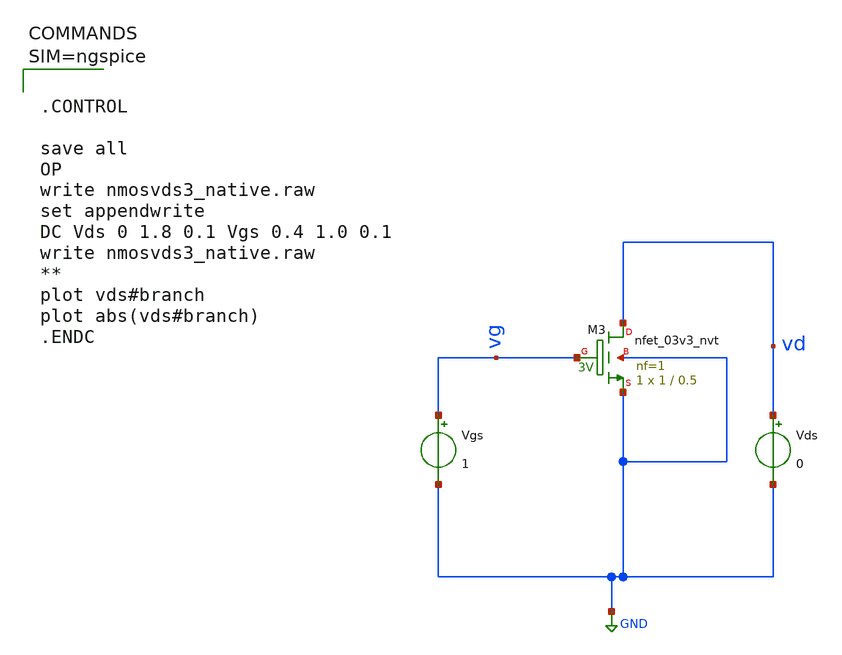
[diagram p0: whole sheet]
** sch_path: work/xschem/nmosvds3_native.sch
**.subckt nmosvds3_native
Vgs vg GND 1
Vds vd GND 0
XM3 vd vg GND GND sky130_fd_pr__nfet_03v3_nvt L=0.5 W=1 nf=1 ad='int((1 + 1)/2) * 1 / 1 * 0.29' as='int((1 + 2)/2) * 1 / 1 * 0.29'
+ pd='2*int((1 + 1)/2) * (1 / 1 + 0.29)' ps='2*int((1 + 2)/2) * (1 / 1 + 0.29)' nrd='0.29 / 1 ' nrs='0.29 / 1 '
+ sa=0 sb=0 sd=0 mult=1 m=1
**** begin user architecture code



.CONTROL

save all
OP
write nmosvds3_native.raw
set appendwrite
DC Vds 0 1.8 0.1 Vgs 0.4 1.0 0.1
write nmosvds3_native.raw
**
plot vds#branch
plot abs(vds#branch)
.ENDC




** opencircuitdesign pdks install
.lib $::SKYWATER_MODELS/sky130.lib.spice tt

**** end user architecture code
**.ends
.GLOBAL GND
.end
